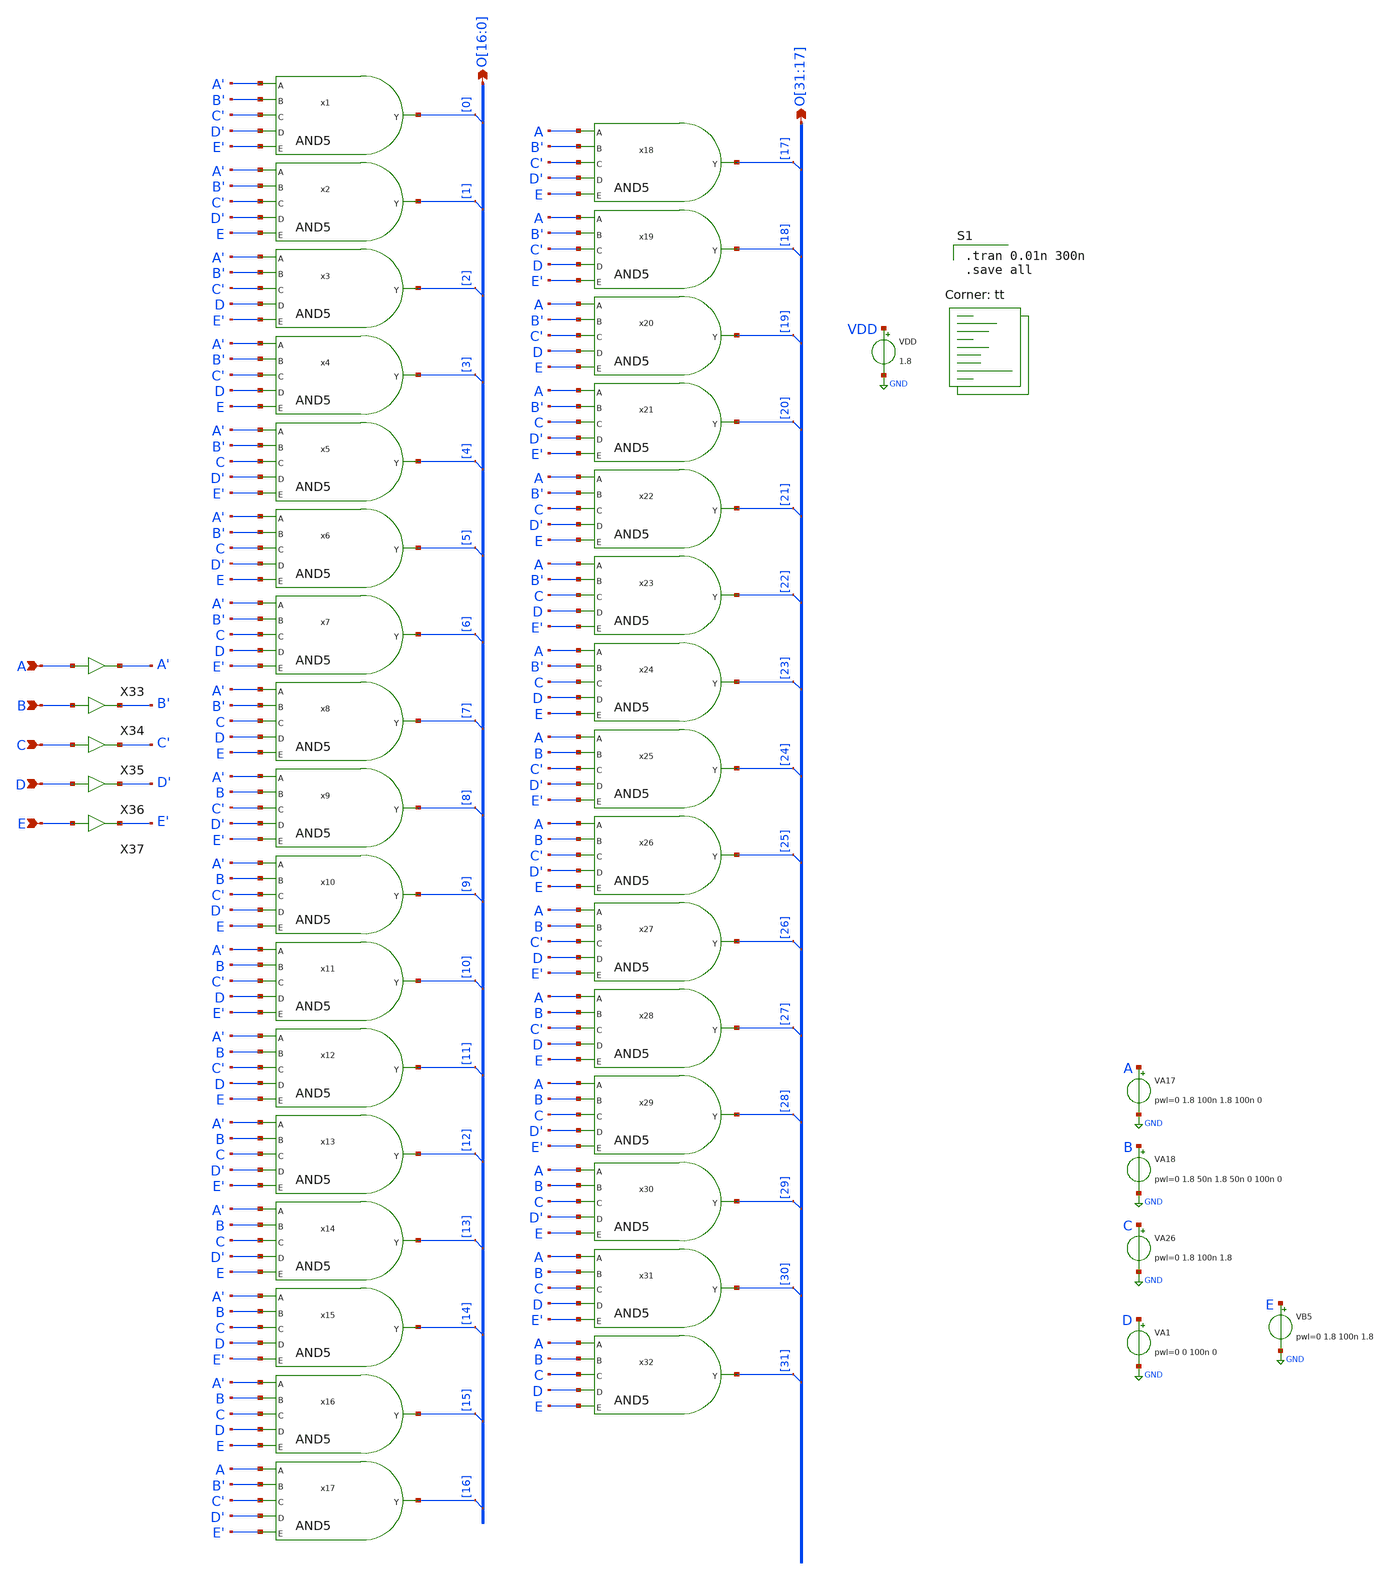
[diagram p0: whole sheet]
** sch_path: gates/Decoder 5x32.sch
**.subckt Decoder 5x32
*+ O[16],O[15],O[14],O[13],O[12],O[11],O[10],O[9],O[8],O[7],O[6],O[5],O[4],O[3],O[2],O[1],O[0] A B C D E O[31],O[30],O[29],O[28],O[27],O[26],O[25],O[24],O[23],O[22],O[21],O[20],O[19],O[18],O[17]
*.opin O[16],O[15],O[14],O[13],O[12],O[11],O[10],O[9],O[8],O[7],O[6],O[5],O[4],O[3],O[2],O[1],O[0]
*.ipin A
*.ipin B
*.ipin C
*.ipin D
*.ipin E
*.opin O[31],O[30],O[29],O[28],O[27],O[26],O[25],O[24],O[23],O[22],O[21],O[20],O[19],O[18],O[17]
x1 A' O[0] B' C' D' E' AND5
x2 A' O[1] B' C' D' E AND5
x3 A' O[2] B' C' D E' AND5
x4 A' O[3] B' C' D E AND5
x5 A' O[4] B' C D' E' AND5
x6 A' O[5] B' C D' E AND5
x7 A' O[6] B' C D E' AND5
x8 A' O[7] B' C D E AND5
x9 A' O[8] B C' D' E' AND5
x10 A' O[9] B C' D' E AND5
x11 A' O[10] B C' D E' AND5
x12 A' O[11] B C' D E AND5
x13 A' O[12] B C D' E' AND5
x14 A' O[13] B C D' E AND5
x15 A' O[14] B C D E' AND5
x16 A' O[15] B C D E AND5
x17 A O[16] B' C' D' E' AND5
x18 A O[17] B' C' D' E AND5
x19 A O[18] B' C' D E' AND5
x20 A O[19] B' C' D E AND5
x21 A O[20] B' C D' E' AND5
x22 A O[21] B' C D' E AND5
x23 A O[22] B' C D E' AND5
x24 A O[23] B' C D E AND5
x25 A O[24] B C' D' E' AND5
x26 A O[25] B C' D' E AND5
x27 A O[26] B C' D E' AND5
x28 A O[27] B C' D E AND5
x29 A O[28] B C D' E' AND5
x30 A O[29] B C D' E AND5
x31 A O[30] B C D E' AND5
x32 A O[31] B C D E AND5
X33 A A' inv_vtc
X34 B B' inv_vtc
X35 C C' inv_vtc
X36 D D' inv_vtc
X37 E E' inv_vtc
* tap: O[16:0] --> O[0]
* tap: O[16:0] --> O[1]
* tap: O[16:0] --> O[2]
* tap: O[16:0] --> O[3]
* tap: O[16:0] --> O[4]
* tap: O[16:0] --> O[5]
* tap: O[16:0] --> O[6]
* tap: O[16:0] --> O[7]
* tap: O[16:0] --> O[8]
* tap: O[16:0] --> O[9]
* tap: O[16:0] --> O[10]
* tap: O[16:0] --> O[11]
* tap: O[16:0] --> O[12]
* tap: O[16:0] --> O[13]
* tap: O[16:0] --> O[14]
* tap: O[16:0] --> O[15]
* tap: O[16:0] --> O[16]
* tap: O[31:17] --> O[17]
* tap: O[31:17] --> O[18]
* tap: O[31:17] --> O[19]
* tap: O[31:17] --> O[20]
* tap: O[31:17] --> O[21]
* tap: O[31:17] --> O[22]
* tap: O[31:17] --> O[23]
* tap: O[31:17] --> O[24]
* tap: O[31:17] --> O[25]
* tap: O[31:17] --> O[26]
* tap: O[31:17] --> O[27]
* tap: O[31:17] --> O[28]
* tap: O[31:17] --> O[29]
* tap: O[31:17] --> O[30]
* tap: O[31:17] --> O[31]
VB5 E GND pwl=0 1.8 100n 1.8
VDD VDD GND 1.8
VA17 A GND pwl=0 1.8 100n 1.8 100n 0
VA18 B GND pwl=0 1.8 50n 1.8 50n 0 100n 0
VA26 C GND pwl=0 1.8 100n 1.8
VA1 D GND pwl=0 0 100n 0
**** begin user architecture code

.tran 0.01n 300n
.save all

.lib $::SKYWATER_MODELS/sky130.lib.spice tt
**** end user architecture code
**.ends

* expanding   symbol:  AND5.sym # of pins=6
** sym_path: gates/AND5.sym
** sch_path: gates/AND5.sch
.subckt AND5 A Y B C D E
*.ipin A
*.ipin B
*.opin Y
*.ipin C
*.ipin D
*.ipin E
XM1 net1 A net2 GND sky130_fd_pr__nfet_01v8 L=0.15 W=1 nf=1 ad='int((nf+1)/2) * W/nf * 0.29' as='int((nf+2)/2)
+ * W/nf * 0.29' pd='2*int((nf+1)/2) * (W/nf + 0.29)' ps='2*int((nf+2)/2) * (W/nf + 0.29)' nrd='0.29 /
+ W' nrs='0.29 / W' sa=0 sb=0 sd=0 mult=1 m=1
XM2 net2 B net3 GND sky130_fd_pr__nfet_01v8 L=0.15 W=1 nf=1 ad='int((nf+1)/2) * W/nf * 0.29' as='int((nf+2)/2)
+ * W/nf * 0.29' pd='2*int((nf+1)/2) * (W/nf + 0.29)' ps='2*int((nf+2)/2) * (W/nf + 0.29)' nrd='0.29 /
+ W' nrs='0.29 / W' sa=0 sb=0 sd=0 mult=1 m=1
XM3 net1 A VDD VDD sky130_fd_pr__pfet_01v8 L=0.15 W=1 nf=1 ad='int((nf+1)/2) * W/nf * 0.29' as='int((nf+2)/2)
+ * W/nf * 0.29' pd='2*int((nf+1)/2) * (W/nf + 0.29)' ps='2*int((nf+2)/2) * (W/nf + 0.29)' nrd='0.29 /
+ W' nrs='0.29 / W' sa=0 sb=0 sd=0 mult=1 m=1
XM4 net1 B VDD VDD sky130_fd_pr__pfet_01v8 L=0.15 W=1 nf=1 ad='int((nf+1)/2) * W/nf * 0.29' as='int((nf+2)/2)
+ * W/nf * 0.29' pd='2*int((nf+1)/2) * (W/nf + 0.29)' ps='2*int((nf+2)/2) * (W/nf + 0.29)' nrd='0.29 /
+ W' nrs='0.29 / W' sa=0 sb=0 sd=0 mult=1 m=1
XM5 net1 C VDD VDD sky130_fd_pr__pfet_01v8 L=0.15 W=1 nf=1 ad='int((nf+1)/2) * W/nf * 0.29' as='int((nf+2)/2)
+ * W/nf * 0.29' pd='2*int((nf+1)/2) * (W/nf + 0.29)' ps='2*int((nf+2)/2) * (W/nf + 0.29)' nrd='0.29 /
+ W' nrs='0.29 / W' sa=0 sb=0 sd=0 mult=1 m=1
XM6 net3 C net4 GND sky130_fd_pr__nfet_01v8 L=0.15 W=1 nf=1 ad='int((nf+1)/2) * W/nf * 0.29' as='int((nf+2)/2)
+ * W/nf * 0.29' pd='2*int((nf+1)/2) * (W/nf + 0.29)' ps='2*int((nf+2)/2) * (W/nf + 0.29)' nrd='0.29 /
+ W' nrs='0.29 / W' sa=0 sb=0 sd=0 mult=1 m=1
XM7 net1 D VDD VDD sky130_fd_pr__pfet_01v8 L=0.15 W=1 nf=1 ad='int((nf+1)/2) * W/nf * 0.29' as='int((nf+2)/2)
+ * W/nf * 0.29' pd='2*int((nf+1)/2) * (W/nf + 0.29)' ps='2*int((nf+2)/2) * (W/nf + 0.29)' nrd='0.29 /
+ W' nrs='0.29 / W' sa=0 sb=0 sd=0 mult=1 m=1
XM8 net4 D GND GND sky130_fd_pr__nfet_01v8 L=0.15 W=1 nf=1 ad='int((nf+1)/2) * W/nf * 0.29' as='int((nf+2)/2)
+ * W/nf * 0.29' pd='2*int((nf+1)/2) * (W/nf + 0.29)' ps='2*int((nf+2)/2) * (W/nf + 0.29)' nrd='0.29 /
+ W' nrs='0.29 / W' sa=0 sb=0 sd=0 mult=1 m=1
XM9 net1 E VDD VDD sky130_fd_pr__pfet_01v8 L=0.15 W=1 nf=1 ad='int((nf+1)/2) * W/nf * 0.29' as='int((nf+2)/2)
+ * W/nf * 0.29' pd='2*int((nf+1)/2) * (W/nf + 0.29)' ps='2*int((nf+2)/2) * (W/nf + 0.29)' nrd='0.29 /
+ W' nrs='0.29 / W' sa=0 sb=0 sd=0 mult=1 m=1
XM10 GND E GND GND sky130_fd_pr__nfet_01v8 L=0.15 W=1 nf=1 ad='int((nf+1)/2) * W/nf * 0.29' as='int((nf+2)/2)
+ * W/nf * 0.29' pd='2*int((nf+1)/2) * (W/nf + 0.29)' ps='2*int((nf+2)/2) * (W/nf + 0.29)' nrd='0.29 /
+ W' nrs='0.29 / W' sa=0 sb=0 sd=0 mult=1 m=1
X1 net1 Y inv_vtc
.ends


* expanding   symbol:  /home/apn/test_xschem_sky130/inv_vtc.sym # of pins=2
** sym_path: gates/inv_vtc.sym
** sch_path: gates/inv_vtc.sch
.subckt inv_vtc A Y
*.ipin A
*.opin Y
XM1 Y A VDD VDD sky130_fd_pr__pfet_01v8 L=0.15 W=2 nf=1 ad='int((nf+1)/2) * W/nf * 0.29' as='int((nf+2)/2)
+ * W/nf * 0.29' pd='2*int((nf+1)/2) * (W/nf + 0.29)' ps='2*int((nf+2)/2) * (W/nf + 0.29)' nrd='0.29 /
+ W' nrs='0.29 / W' sa=0 sb=0 sd=0 mult=1 m=1
XM2 Y A GND GND sky130_fd_pr__nfet_01v8 L=0.15 W=1 nf=1 ad='int((nf+1)/2) * W/nf * 0.29' as='int((nf+2)/2)
+ * W/nf * 0.29' pd='2*int((nf+1)/2) * (W/nf + 0.29)' ps='2*int((nf+2)/2) * (W/nf + 0.29)' nrd='0.29 /
+ W' nrs='0.29 / W' sa=0 sb=0 sd=0 mult=1 m=1
.ends

.GLOBAL GND
.GLOBAL VDD
.end
